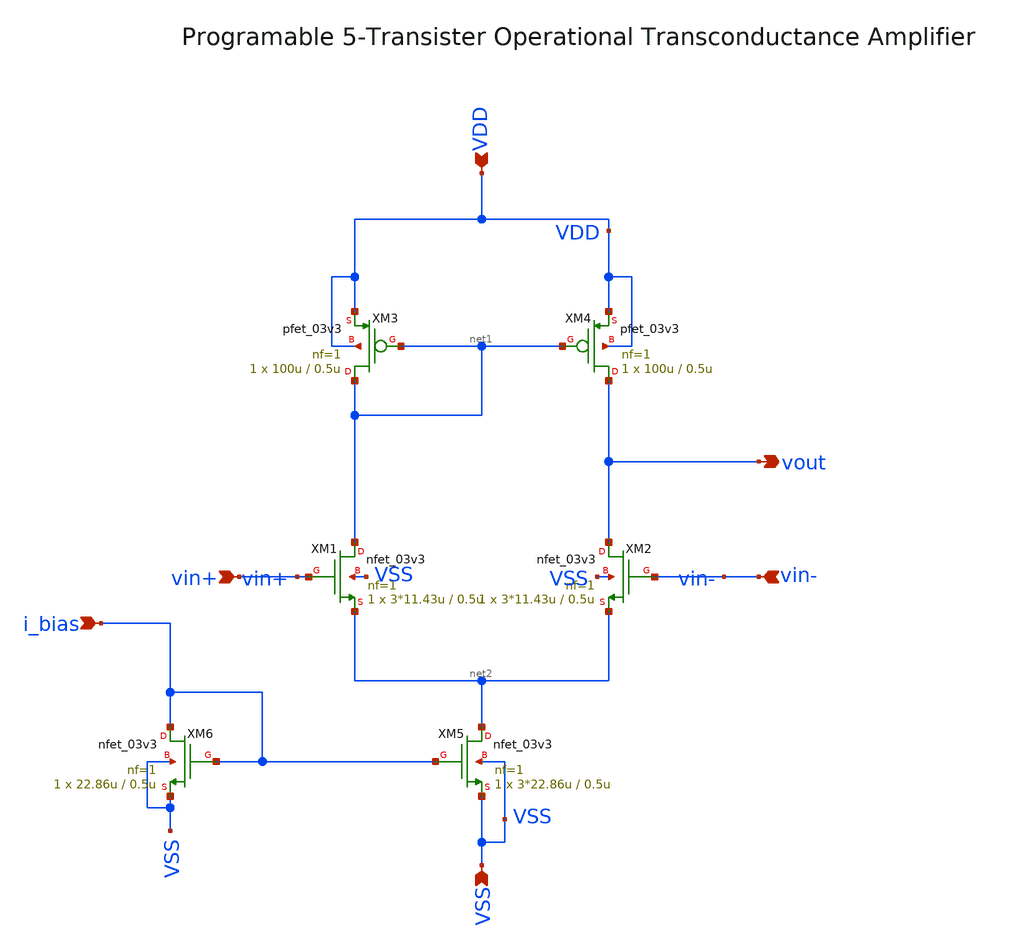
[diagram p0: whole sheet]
** sch_path: designs/libs/core_amps/ota_5t/5tOTA_programable.sch
**.subckt 5tOTA_programable VDD vout i_bias vin+ vin- VSS
*.ipin VDD
*.opin vout
*.ipin i_bias
*.ipin vin+
*.ipin vin-
*.ipin VSS
XM1 net1 vin+ net2 VSS nfet_03v3 L=0.5u W=3*11.43u nf=1 ad='int((nf+1)/2) * W/nf * 0.18u' as='int((nf+2)/2) * W/nf * 0.18u'
+ pd='2*int((nf+1)/2) * (W/nf + 0.18u)' ps='2*int((nf+2)/2) * (W/nf + 0.18u)' nrd='0.18u / W' nrs='0.18u / W'
+ sa=0 sb=0 sd=0 m=1
XM2 vout vin- net2 VSS nfet_03v3 L=0.5u W=3*11.43u nf=1 ad='int((nf+1)/2) * W/nf * 0.18u' as='int((nf+2)/2) * W/nf * 0.18u'
+ pd='2*int((nf+1)/2) * (W/nf + 0.18u)' ps='2*int((nf+2)/2) * (W/nf + 0.18u)' nrd='0.18u / W' nrs='0.18u / W'
+ sa=0 sb=0 sd=0 m=1
XM3 net1 net1 VDD VDD pfet_03v3 L=0.5u W=100u nf=1 ad='int((nf+1)/2) * W/nf * 0.18u' as='int((nf+2)/2) * W/nf * 0.18u'
+ pd='2*int((nf+1)/2) * (W/nf + 0.18u)' ps='2*int((nf+2)/2) * (W/nf + 0.18u)' nrd='0.18u / W' nrs='0.18u / W'
+ sa=0 sb=0 sd=0 m=1
XM4 vout net1 VDD VDD pfet_03v3 L=0.5u W=100u nf=1 ad='int((nf+1)/2) * W/nf * 0.18u' as='int((nf+2)/2) * W/nf * 0.18u'
+ pd='2*int((nf+1)/2) * (W/nf + 0.18u)' ps='2*int((nf+2)/2) * (W/nf + 0.18u)' nrd='0.18u / W' nrs='0.18u / W'
+ sa=0 sb=0 sd=0 m=1
XM5 net2 i_bias VSS VSS nfet_03v3 L=0.5u W=3*22.86u nf=1 ad='int((nf+1)/2) * W/nf * 0.18u' as='int((nf+2)/2) * W/nf * 0.18u'
+ pd='2*int((nf+1)/2) * (W/nf + 0.18u)' ps='2*int((nf+2)/2) * (W/nf + 0.18u)' nrd='0.18u / W' nrs='0.18u / W'
+ sa=0 sb=0 sd=0 m=1
XM6 i_bias i_bias VSS VSS nfet_03v3 L=0.5u W=22.86u nf=1 ad='int((nf+1)/2) * W/nf * 0.18u' as='int((nf+2)/2) * W/nf * 0.18u'
+ pd='2*int((nf+1)/2) * (W/nf + 0.18u)' ps='2*int((nf+2)/2) * (W/nf + 0.18u)' nrd='0.18u / W' nrs='0.18u / W'
+ sa=0 sb=0 sd=0 m=1
**.ends
.end
